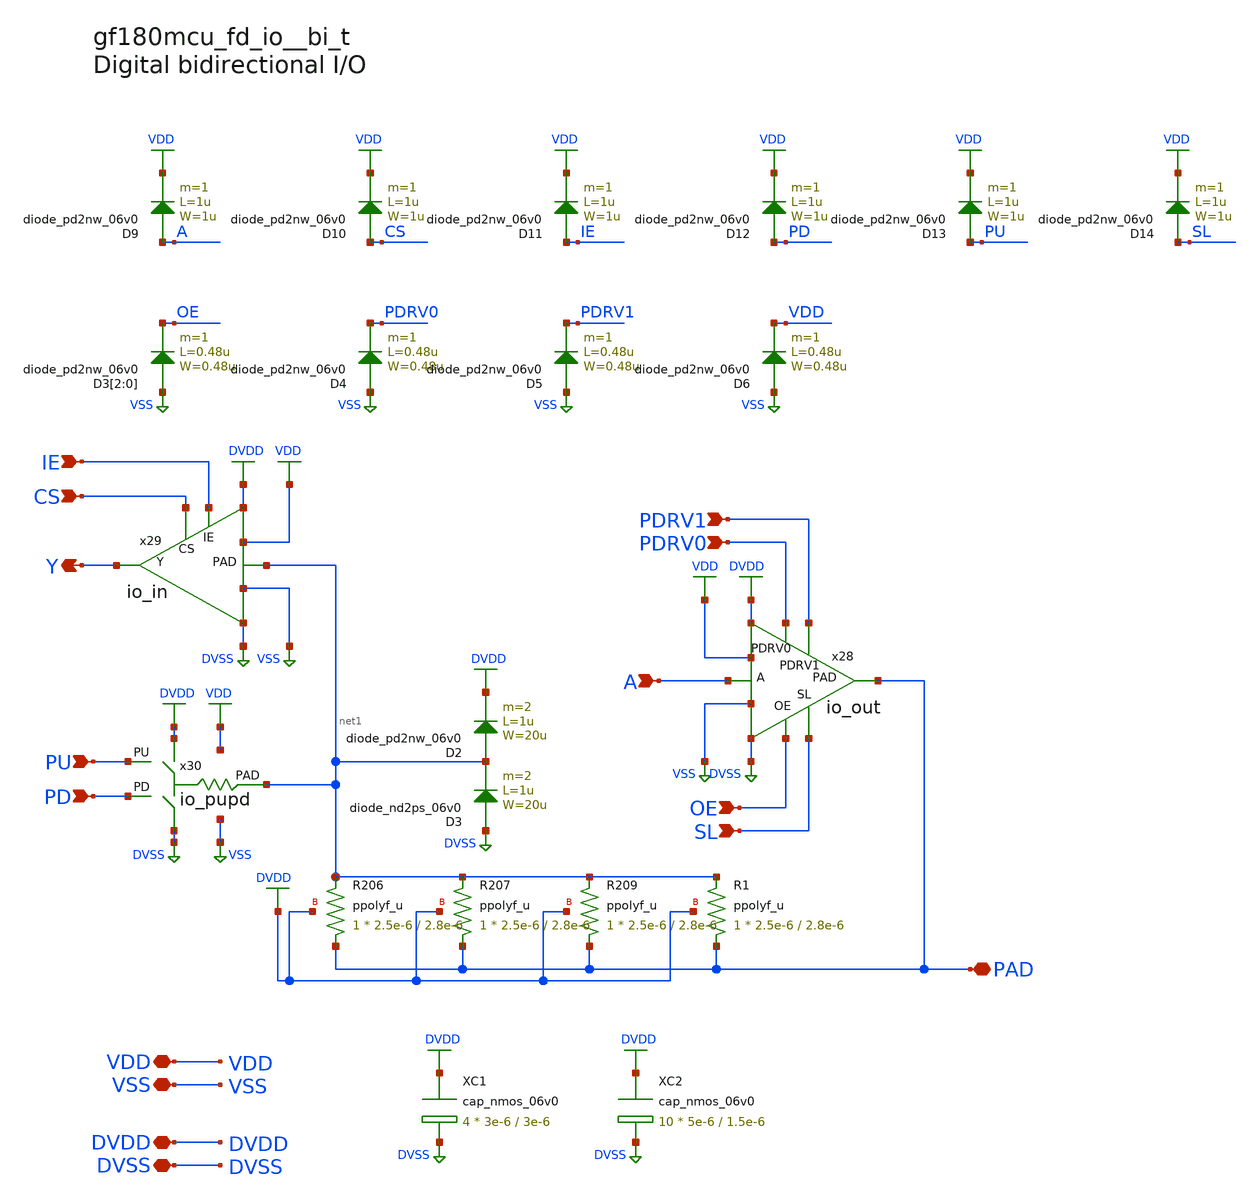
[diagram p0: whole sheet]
** sch_path: cells/bi_t/gf180mcu_fd_io__bi_t.sch
* Copyright 2023 David Mitchell Bailey
* Licensed under the Apache License, Version 2.0 (the "License");
* you may not use this file except in compliance with the License.
* You may obtain a copy of the License at
* https://www.apache.org/licenses/LICENSE-2.0
* Unless required by applicable law or agreed to in writing, software
* distributed under the License is distributed on an "AS IS" BASIS,
* WITHOUT WARRANTIES OR CONDITIONS OF ANY KIND, either express or implied.
* See the License for the specific language governing permissions and
* limitations under the License.
**.subckt gf180mcu_fd_io__bi_t A VDD Y VSS DVDD DVSS PU PD PDRV0 PDRV1 SL OE CS IE PAD
*.ipin A
*.iopin VDD
*.opin Y
*.iopin VSS
*.iopin DVDD
*.iopin DVSS
*.ipin PU
*.ipin PD
*.ipin PDRV0
*.ipin PDRV1
*.ipin SL
*.ipin OE
*.ipin CS
*.ipin IE
*.iopin PAD
XR206 PAD net1 DVDD ppolyf_u r_width=2.5e-6 r_length=2.8e-6 m=1
XR207 PAD net1 DVDD ppolyf_u r_width=2.5e-6 r_length=2.8e-6 m=1
XR209 PAD net1 DVDD ppolyf_u r_width=2.5e-6 r_length=2.8e-6 m=1
XR1 PAD net1 DVDD ppolyf_u r_width=2.5e-6 r_length=2.8e-6 m=1
x28 OE A SL PDRV0 PDRV1 PAD DVDD DVSS VDD VSS io_out
x29 net1 IE CS Y DVDD DVSS VDD VSS io_in
x30 DVDD DVSS PU PD net1 VDD VSS io_pupd
XC1 DVDD DVSS cap_nmos_06v0 c_width=3e-6 c_length=3e-6 m=4
XC2 DVDD DVSS cap_nmos_06v0 c_width=5e-6 c_length=1.5e-6 m=10
D3 DVSS net1 diode_nd2ps_06v0 area='20u * 1u ' pj='2*20u + 2*1u ' m=2
D2 net1 DVDD diode_pd2nw_06v0 area='20u * 1u ' pj='2*20u + 2*1u ' m=2
D3[2] VSS OE diode_pd2nw_06v0 area='0.48u * 0.48u ' pj='2*0.48u + 2*0.48u ' m=1
D3[1] VSS OE diode_pd2nw_06v0 area='0.48u * 0.48u ' pj='2*0.48u + 2*0.48u ' m=1
D3[0] VSS OE diode_pd2nw_06v0 area='0.48u * 0.48u ' pj='2*0.48u + 2*0.48u ' m=1
D4 VSS PDRV0 diode_pd2nw_06v0 area='0.48u * 0.48u ' pj='2*0.48u + 2*0.48u ' m=1
D5 VSS PDRV1 diode_pd2nw_06v0 area='0.48u * 0.48u ' pj='2*0.48u + 2*0.48u ' m=1
D6 VSS VDD diode_pd2nw_06v0 area='0.48u * 0.48u ' pj='2*0.48u + 2*0.48u ' m=1
D9 A VDD diode_pd2nw_06v0 area='1u * 1u ' pj='2*1u + 2*1u ' m=1
D10 CS VDD diode_pd2nw_06v0 area='1u * 1u ' pj='2*1u + 2*1u ' m=1
D11 IE VDD diode_pd2nw_06v0 area='1u * 1u ' pj='2*1u + 2*1u ' m=1
D12 PD VDD diode_pd2nw_06v0 area='1u * 1u ' pj='2*1u + 2*1u ' m=1
D13 PU VDD diode_pd2nw_06v0 area='1u * 1u ' pj='2*1u + 2*1u ' m=1
D14 SL VDD diode_pd2nw_06v0 area='1u * 1u ' pj='2*1u + 2*1u ' m=1
**.ends
.GLOBAL DVSS
.GLOBAL DVDD
.GLOBAL VDD
.GLOBAL VSS
.end
